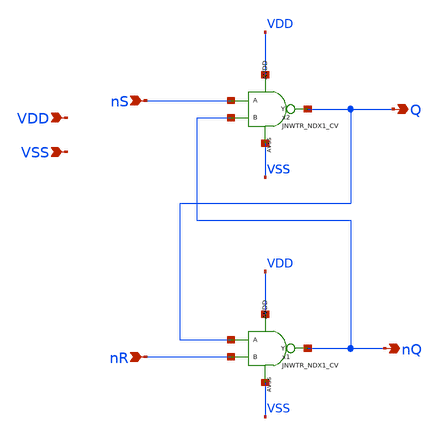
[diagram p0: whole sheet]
** sch_path: design/JNW_GR05_SKY130A/fuckRepo/RS-latch.sch
**.subckt RS-latch VDD VSS nS nR Q nQ
*.ipin VDD
*.ipin VSS
*.ipin nS
*.ipin nR
*.opin Q
*.opin nQ
x2 nS nQ Q VDD VSS JNWTR_NDX1_CV
x1 Q nR nQ VDD VSS JNWTR_NDX1_CV
**.ends
.end
